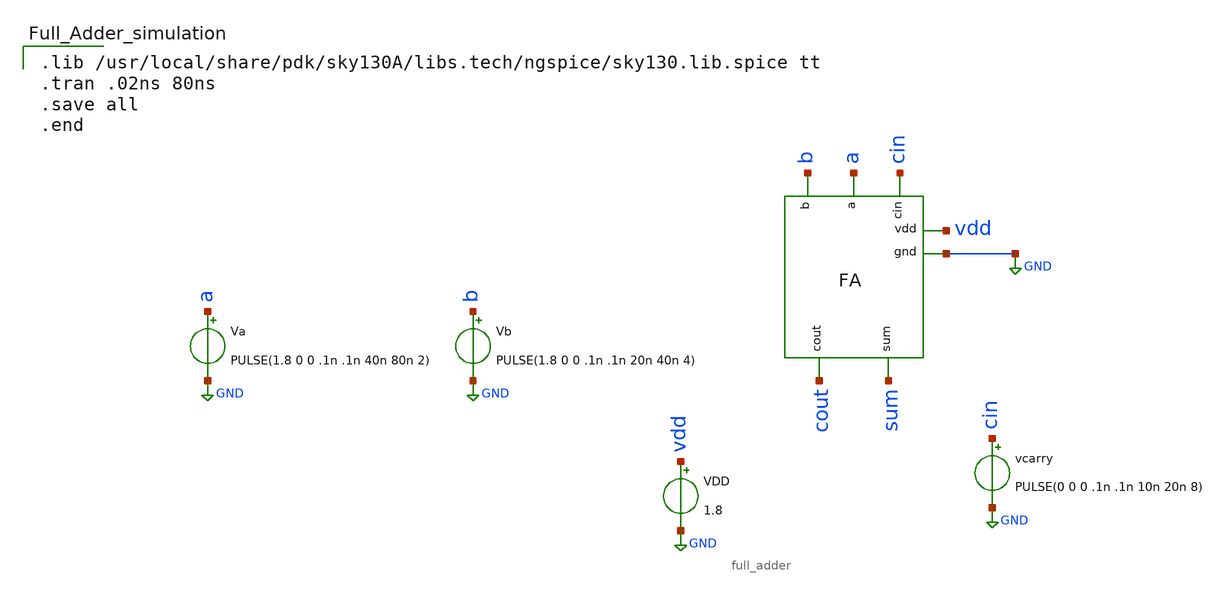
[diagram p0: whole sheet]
** sch_path: Projects/Design_and_Analysis_of_8-bit_Carry_Select_Adder_Schematic_Design_Layout_Design_and_LVS_Validation_using_SKY130PDK/assets/files/schematic/fa_tb.sch
**.subckt fa_tb
VDD vdd GND 1.8
vcarry cin GND PULSE(0 0 0 .1n .1n 10n 20n 8)
Va a GND PULSE(1.8 0 0 .1n .1n 40n 80n 2)
Vb b GND PULSE(1.8 0 0 .1n .1n 20n 40n 4)
x1 sum cout vdd GND cin a b full_adder
**** begin user architecture code

.lib /usr/local/share/pdk/sky130A/libs.tech/ngspice/sky130.lib.spice tt
.tran .02ns 80ns
.save all
.end

**** end user architecture code
**.ends

* expanding   symbol:  full_adder.sym # of pins=7
** sym_path: Projects/Design_and_Analysis_of_8-bit_Carry_Select_Adder_Schematic_Design_Layout_Design_and_LVS_Validation_using_SKY130PDK/assets/files/schematic/full_adder.sym
** sch_path: Projects/Design_and_Analysis_of_8-bit_Carry_Select_Adder_Schematic_Design_Layout_Design_and_LVS_Validation_using_SKY130PDK/assets/files/schematic/full_adder.sch
.subckt full_adder sum cout vdd gnd cin a b
*.ipin a
*.ipin b
*.ipin cin
*.opin cout
*.opin sum
*.ipin vdd
*.ipin gnd
XM27 sum net1 vdd vdd sky130_fd_pr__pfet_01v8 L=0.15 W=2 nf=1 ad='int((nf+1)/2) * W/nf * 0.29' as='int((nf+2)/2) * W/nf * 0.29'
+ pd='2*int((nf+1)/2) * (W/nf + 0.29)' ps='2*int((nf+2)/2) * (W/nf + 0.29)' nrd='0.29 / W' nrs='0.29 / W'
+ sa=0 sb=0 sd=0 mult=1 m=1
XM28 sum net1 gnd gnd sky130_fd_pr__nfet_01v8 L=0.15 W=1 nf=1 ad='int((nf+1)/2) * W/nf * 0.29' as='int((nf+2)/2) * W/nf * 0.29'
+ pd='2*int((nf+1)/2) * (W/nf + 0.29)' ps='2*int((nf+2)/2) * (W/nf + 0.29)' nrd='0.29 / W' nrs='0.29 / W'
+ sa=0 sb=0 sd=0 mult=1 m=1
XM11 cout net2 vdd vdd sky130_fd_pr__pfet_01v8 L=0.15 W=2 nf=1 ad='int((nf+1)/2) * W/nf * 0.29' as='int((nf+2)/2) * W/nf * 0.29'
+ pd='2*int((nf+1)/2) * (W/nf + 0.29)' ps='2*int((nf+2)/2) * (W/nf + 0.29)' nrd='0.29 / W' nrs='0.29 / W'
+ sa=0 sb=0 sd=0 mult=1 m=1
XM12 cout net2 gnd gnd sky130_fd_pr__nfet_01v8 L=0.15 W=1 nf=1 ad='int((nf+1)/2) * W/nf * 0.29' as='int((nf+2)/2) * W/nf * 0.29'
+ pd='2*int((nf+1)/2) * (W/nf + 0.29)' ps='2*int((nf+2)/2) * (W/nf + 0.29)' nrd='0.29 / W' nrs='0.29 / W'
+ sa=0 sb=0 sd=0 mult=1 m=1
XM1 net2 cin net4 gnd sky130_fd_pr__nfet_01v8 L=0.15 W=2 nf=1 ad='int((nf+1)/2) * W/nf * 0.29' as='int((nf+2)/2) * W/nf * 0.29'
+ pd='2*int((nf+1)/2) * (W/nf + 0.29)' ps='2*int((nf+2)/2) * (W/nf + 0.29)' nrd='0.29 / W' nrs='0.29 / W'
+ sa=0 sb=0 sd=0 mult=1 m=1
XM2 net3 a vdd vdd sky130_fd_pr__pfet_01v8 L=0.15 W=4 nf=1 ad='int((nf+1)/2) * W/nf * 0.29' as='int((nf+2)/2) * W/nf * 0.29'
+ pd='2*int((nf+1)/2) * (W/nf + 0.29)' ps='2*int((nf+2)/2) * (W/nf + 0.29)' nrd='0.29 / W' nrs='0.29 / W'
+ sa=0 sb=0 sd=0 mult=1 m=1
XM3 net3 b vdd vdd sky130_fd_pr__pfet_01v8 L=0.15 W=4 nf=1 ad='int((nf+1)/2) * W/nf * 0.29' as='int((nf+2)/2) * W/nf * 0.29'
+ pd='2*int((nf+1)/2) * (W/nf + 0.29)' ps='2*int((nf+2)/2) * (W/nf + 0.29)' nrd='0.29 / W' nrs='0.29 / W'
+ sa=0 sb=0 sd=0 mult=1 m=1
XM4 net2 cin net3 vdd sky130_fd_pr__pfet_01v8 L=0.15 W=4 nf=1 ad='int((nf+1)/2) * W/nf * 0.29' as='int((nf+2)/2) * W/nf * 0.29'
+ pd='2*int((nf+1)/2) * (W/nf + 0.29)' ps='2*int((nf+2)/2) * (W/nf + 0.29)' nrd='0.29 / W' nrs='0.29 / W'
+ sa=0 sb=0 sd=0 mult=1 m=1
XM5 net4 a gnd gnd sky130_fd_pr__nfet_01v8 L=0.15 W=2 nf=1 ad='int((nf+1)/2) * W/nf * 0.29' as='int((nf+2)/2) * W/nf * 0.29'
+ pd='2*int((nf+1)/2) * (W/nf + 0.29)' ps='2*int((nf+2)/2) * (W/nf + 0.29)' nrd='0.29 / W' nrs='0.29 / W'
+ sa=0 sb=0 sd=0 mult=1 m=1
XM6 net4 b gnd gnd sky130_fd_pr__nfet_01v8 L=0.15 W=2 nf=1 ad='int((nf+1)/2) * W/nf * 0.29' as='int((nf+2)/2) * W/nf * 0.29'
+ pd='2*int((nf+1)/2) * (W/nf + 0.29)' ps='2*int((nf+2)/2) * (W/nf + 0.29)' nrd='0.29 / W' nrs='0.29 / W'
+ sa=0 sb=0 sd=0 mult=1 m=1
XM7 net2 a net6 vdd sky130_fd_pr__pfet_01v8 L=0.15 W=4 nf=1 ad='int((nf+1)/2) * W/nf * 0.29' as='int((nf+2)/2) * W/nf * 0.29'
+ pd='2*int((nf+1)/2) * (W/nf + 0.29)' ps='2*int((nf+2)/2) * (W/nf + 0.29)' nrd='0.29 / W' nrs='0.29 / W'
+ sa=0 sb=0 sd=0 mult=1 m=1
XM8 net6 b vdd vdd sky130_fd_pr__pfet_01v8 L=0.15 W=4 nf=1 ad='int((nf+1)/2) * W/nf * 0.29' as='int((nf+2)/2) * W/nf * 0.29'
+ pd='2*int((nf+1)/2) * (W/nf + 0.29)' ps='2*int((nf+2)/2) * (W/nf + 0.29)' nrd='0.29 / W' nrs='0.29 / W'
+ sa=0 sb=0 sd=0 mult=1 m=1
XM9 net2 a net5 gnd sky130_fd_pr__nfet_01v8 L=0.15 W=2 nf=1 ad='int((nf+1)/2) * W/nf * 0.29' as='int((nf+2)/2) * W/nf * 0.29'
+ pd='2*int((nf+1)/2) * (W/nf + 0.29)' ps='2*int((nf+2)/2) * (W/nf + 0.29)' nrd='0.29 / W' nrs='0.29 / W'
+ sa=0 sb=0 sd=0 mult=1 m=1
XM10 net5 b gnd gnd sky130_fd_pr__nfet_01v8 L=0.15 W=2 nf=1 ad='int((nf+1)/2) * W/nf * 0.29' as='int((nf+2)/2) * W/nf * 0.29'
+ pd='2*int((nf+1)/2) * (W/nf + 0.29)' ps='2*int((nf+2)/2) * (W/nf + 0.29)' nrd='0.29 / W' nrs='0.29 / W'
+ sa=0 sb=0 sd=0 mult=1 m=1
XM13 net8 a vdd vdd sky130_fd_pr__pfet_01v8 L=0.15 W=4 nf=1 ad='int((nf+1)/2) * W/nf * 0.29' as='int((nf+2)/2) * W/nf * 0.29'
+ pd='2*int((nf+1)/2) * (W/nf + 0.29)' ps='2*int((nf+2)/2) * (W/nf + 0.29)' nrd='0.29 / W' nrs='0.29 / W'
+ sa=0 sb=0 sd=0 mult=1 m=1
XM14 net8 b vdd vdd sky130_fd_pr__pfet_01v8 L=0.15 W=4 nf=1 ad='int((nf+1)/2) * W/nf * 0.29' as='int((nf+2)/2) * W/nf * 0.29'
+ pd='2*int((nf+1)/2) * (W/nf + 0.29)' ps='2*int((nf+2)/2) * (W/nf + 0.29)' nrd='0.29 / W' nrs='0.29 / W'
+ sa=0 sb=0 sd=0 mult=1 m=1
XM15 net8 cin vdd vdd sky130_fd_pr__pfet_01v8 L=0.15 W=4 nf=1 ad='int((nf+1)/2) * W/nf * 0.29' as='int((nf+2)/2) * W/nf * 0.29'
+ pd='2*int((nf+1)/2) * (W/nf + 0.29)' ps='2*int((nf+2)/2) * (W/nf + 0.29)' nrd='0.29 / W' nrs='0.29 / W'
+ sa=0 sb=0 sd=0 mult=1 m=1
XM16 net7 a gnd gnd sky130_fd_pr__nfet_01v8 L=0.15 W=2 nf=1 ad='int((nf+1)/2) * W/nf * 0.29' as='int((nf+2)/2) * W/nf * 0.29'
+ pd='2*int((nf+1)/2) * (W/nf + 0.29)' ps='2*int((nf+2)/2) * (W/nf + 0.29)' nrd='0.29 / W' nrs='0.29 / W'
+ sa=0 sb=0 sd=0 mult=1 m=1
XM17 net7 b gnd gnd sky130_fd_pr__nfet_01v8 L=0.15 W=2 nf=1 ad='int((nf+1)/2) * W/nf * 0.29' as='int((nf+2)/2) * W/nf * 0.29'
+ pd='2*int((nf+1)/2) * (W/nf + 0.29)' ps='2*int((nf+2)/2) * (W/nf + 0.29)' nrd='0.29 / W' nrs='0.29 / W'
+ sa=0 sb=0 sd=0 mult=1 m=1
XM18 net7 cin gnd gnd sky130_fd_pr__nfet_01v8 L=0.15 W=2 nf=1 ad='int((nf+1)/2) * W/nf * 0.29' as='int((nf+2)/2) * W/nf * 0.29'
+ pd='2*int((nf+1)/2) * (W/nf + 0.29)' ps='2*int((nf+2)/2) * (W/nf + 0.29)' nrd='0.29 / W' nrs='0.29 / W'
+ sa=0 sb=0 sd=0 mult=1 m=1
XM19 net1 net2 net7 gnd sky130_fd_pr__nfet_01v8 L=0.15 W=2 nf=1 ad='int((nf+1)/2) * W/nf * 0.29' as='int((nf+2)/2) * W/nf * 0.29'
+ pd='2*int((nf+1)/2) * (W/nf + 0.29)' ps='2*int((nf+2)/2) * (W/nf + 0.29)' nrd='0.29 / W' nrs='0.29 / W'
+ sa=0 sb=0 sd=0 mult=1 m=1
XM20 net1 net2 net8 vdd sky130_fd_pr__pfet_01v8 L=0.15 W=4 nf=1 ad='int((nf+1)/2) * W/nf * 0.29' as='int((nf+2)/2) * W/nf * 0.29'
+ pd='2*int((nf+1)/2) * (W/nf + 0.29)' ps='2*int((nf+2)/2) * (W/nf + 0.29)' nrd='0.29 / W' nrs='0.29 / W'
+ sa=0 sb=0 sd=0 mult=1 m=1
XM21 net1 cin net10 vdd sky130_fd_pr__pfet_01v8 L=0.15 W=6 nf=1 ad='int((nf+1)/2) * W/nf * 0.29' as='int((nf+2)/2) * W/nf * 0.29'
+ pd='2*int((nf+1)/2) * (W/nf + 0.29)' ps='2*int((nf+2)/2) * (W/nf + 0.29)' nrd='0.29 / W' nrs='0.29 / W'
+ sa=0 sb=0 sd=0 mult=1 m=1
XM22 net10 b net9 vdd sky130_fd_pr__pfet_01v8 L=0.15 W=6 nf=1 ad='int((nf+1)/2) * W/nf * 0.29' as='int((nf+2)/2) * W/nf * 0.29'
+ pd='2*int((nf+1)/2) * (W/nf + 0.29)' ps='2*int((nf+2)/2) * (W/nf + 0.29)' nrd='0.29 / W' nrs='0.29 / W'
+ sa=0 sb=0 sd=0 mult=1 m=1
XM23 net9 a vdd vdd sky130_fd_pr__pfet_01v8 L=0.15 W=6 nf=1 ad='int((nf+1)/2) * W/nf * 0.29' as='int((nf+2)/2) * W/nf * 0.29'
+ pd='2*int((nf+1)/2) * (W/nf + 0.29)' ps='2*int((nf+2)/2) * (W/nf + 0.29)' nrd='0.29 / W' nrs='0.29 / W'
+ sa=0 sb=0 sd=0 mult=1 m=1
XM24 net1 cin net12 gnd sky130_fd_pr__nfet_01v8 L=0.15 W=3 nf=1 ad='int((nf+1)/2) * W/nf * 0.29' as='int((nf+2)/2) * W/nf * 0.29'
+ pd='2*int((nf+1)/2) * (W/nf + 0.29)' ps='2*int((nf+2)/2) * (W/nf + 0.29)' nrd='0.29 / W' nrs='0.29 / W'
+ sa=0 sb=0 sd=0 mult=1 m=1
XM25 net12 b net11 gnd sky130_fd_pr__nfet_01v8 L=0.15 W=3 nf=1 ad='int((nf+1)/2) * W/nf * 0.29' as='int((nf+2)/2) * W/nf * 0.29'
+ pd='2*int((nf+1)/2) * (W/nf + 0.29)' ps='2*int((nf+2)/2) * (W/nf + 0.29)' nrd='0.29 / W' nrs='0.29 / W'
+ sa=0 sb=0 sd=0 mult=1 m=1
XM26 net11 a gnd gnd sky130_fd_pr__nfet_01v8 L=0.15 W=3 nf=1 ad='int((nf+1)/2) * W/nf * 0.29' as='int((nf+2)/2) * W/nf * 0.29'
+ pd='2*int((nf+1)/2) * (W/nf + 0.29)' ps='2*int((nf+2)/2) * (W/nf + 0.29)' nrd='0.29 / W' nrs='0.29 / W'
+ sa=0 sb=0 sd=0 mult=1 m=1
.ends

.GLOBAL GND
.end
